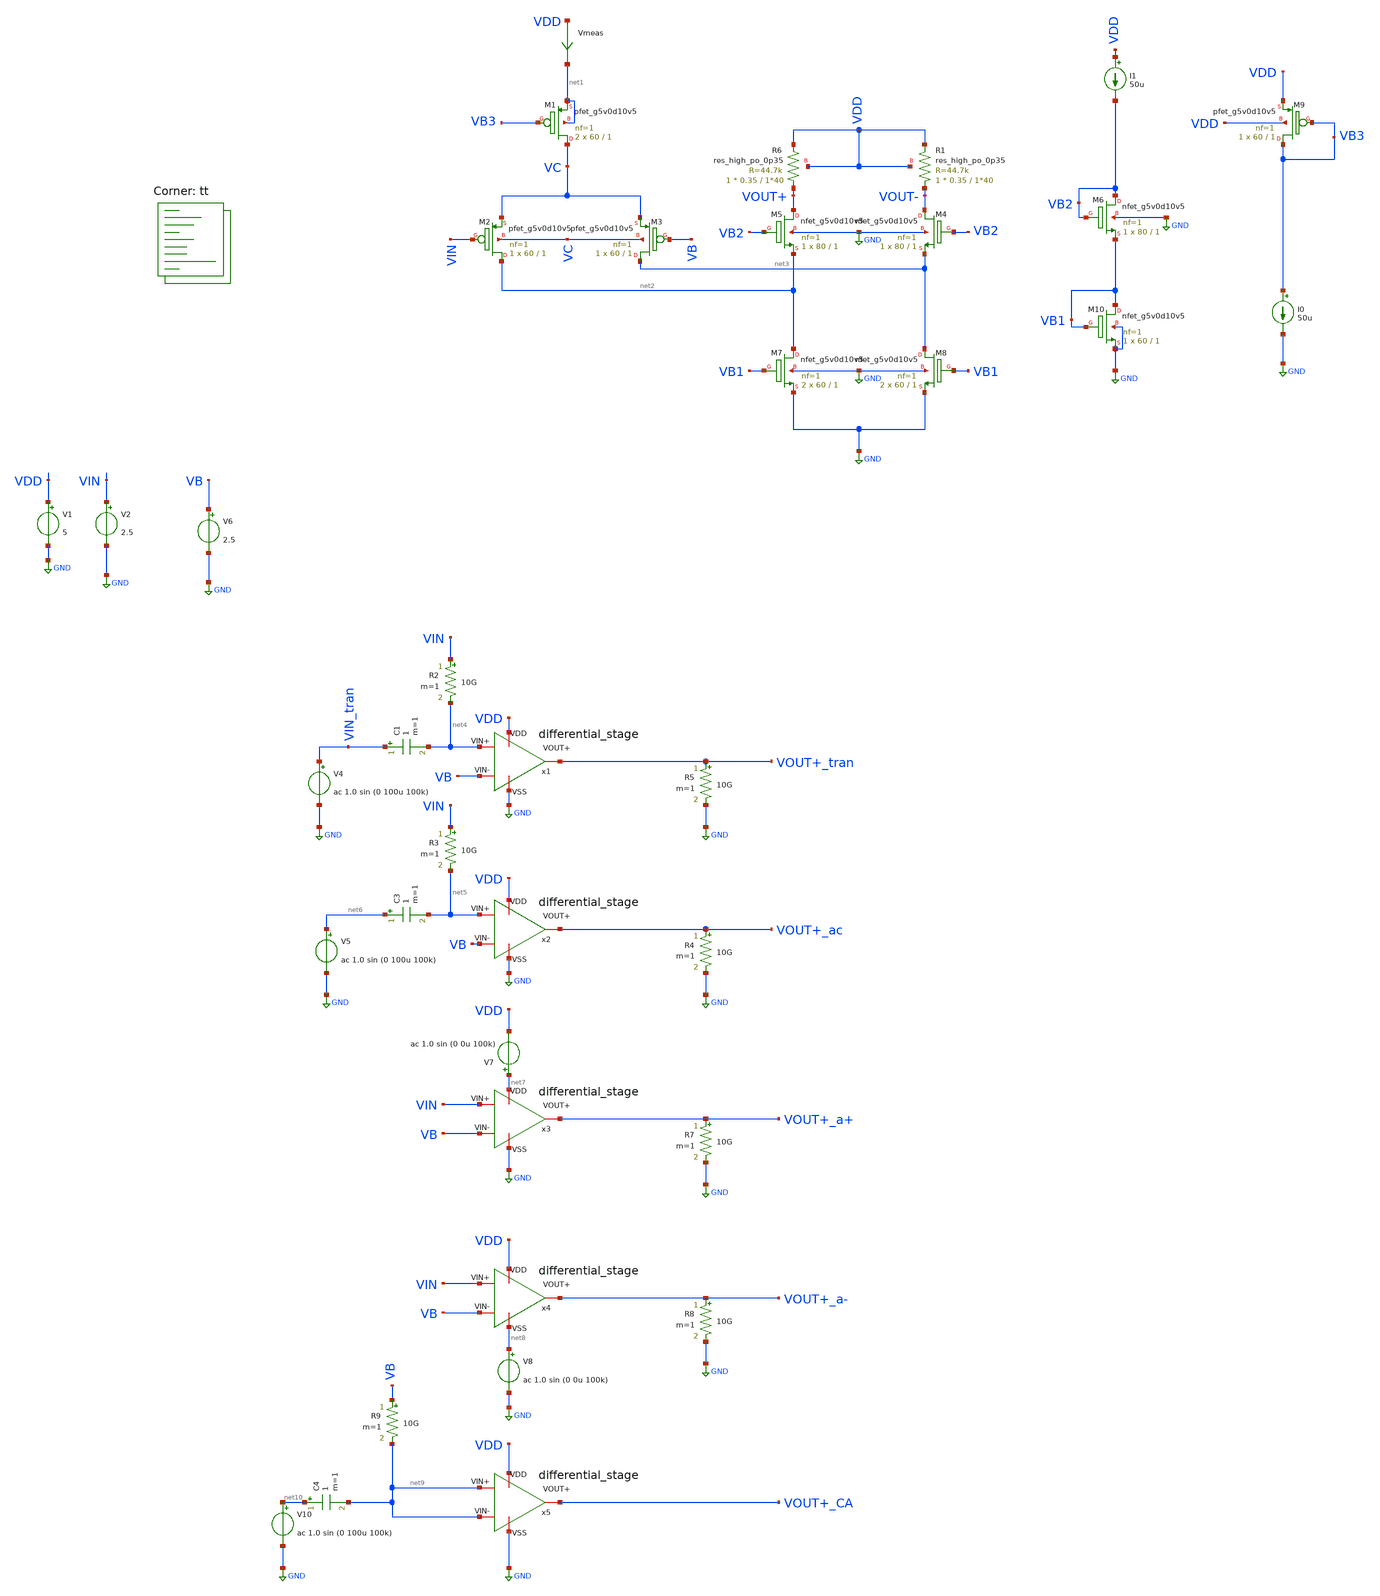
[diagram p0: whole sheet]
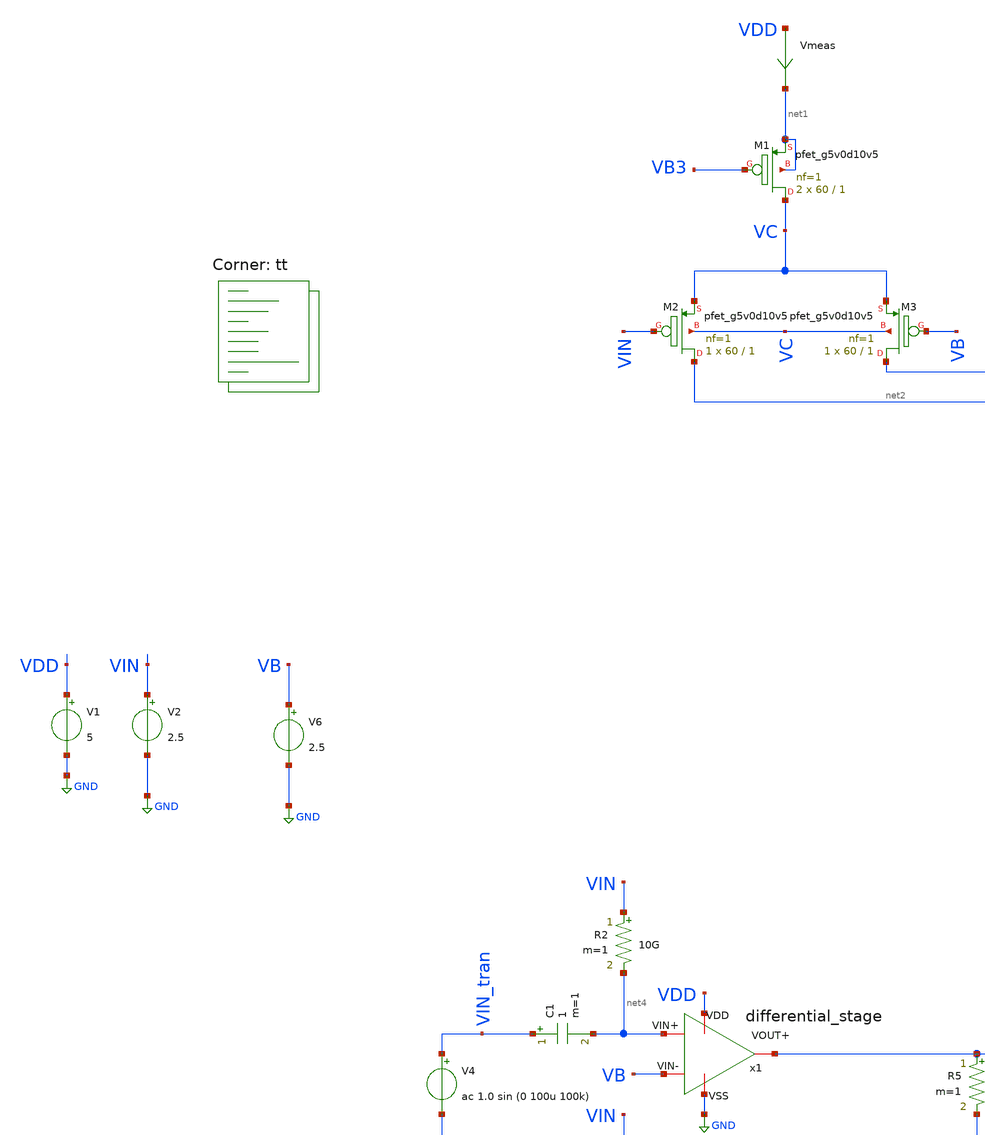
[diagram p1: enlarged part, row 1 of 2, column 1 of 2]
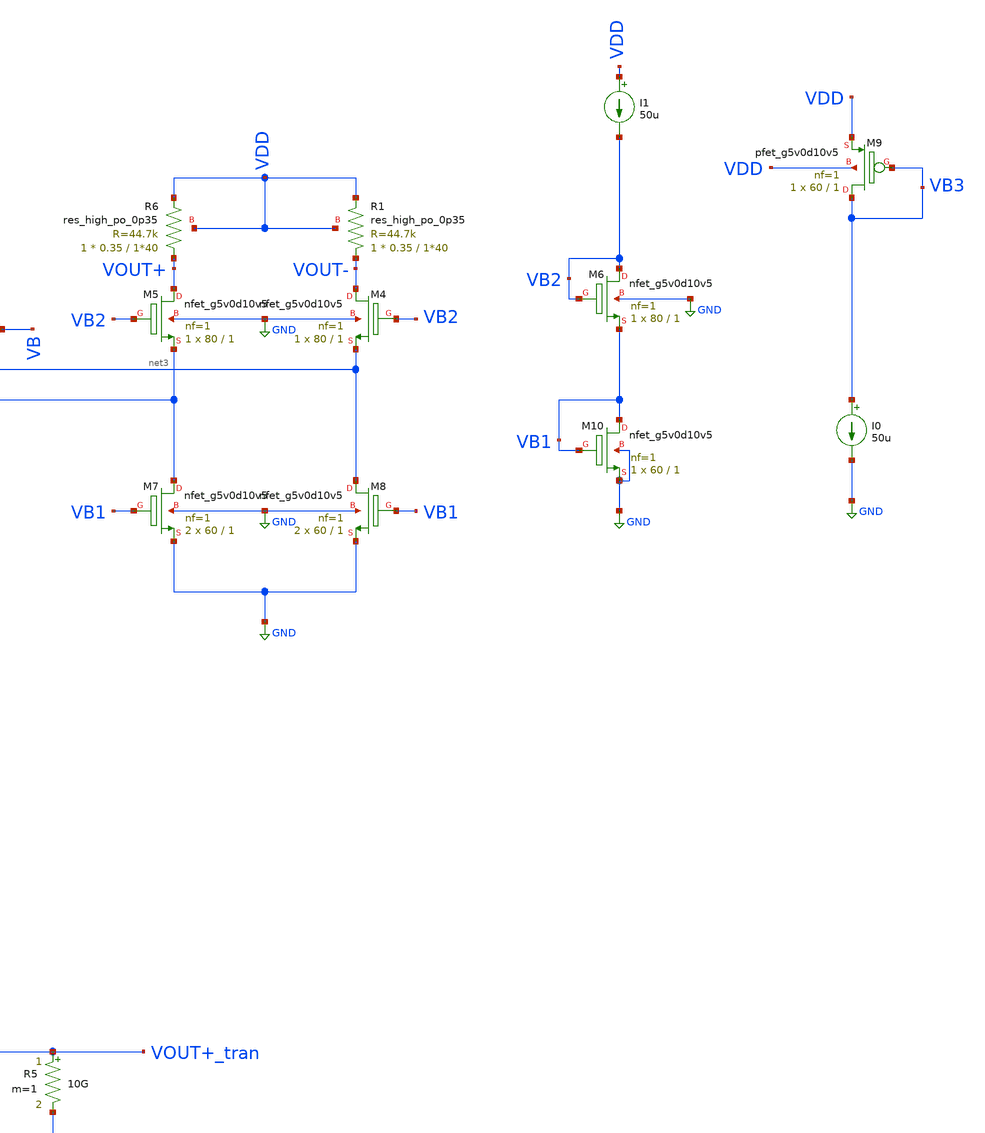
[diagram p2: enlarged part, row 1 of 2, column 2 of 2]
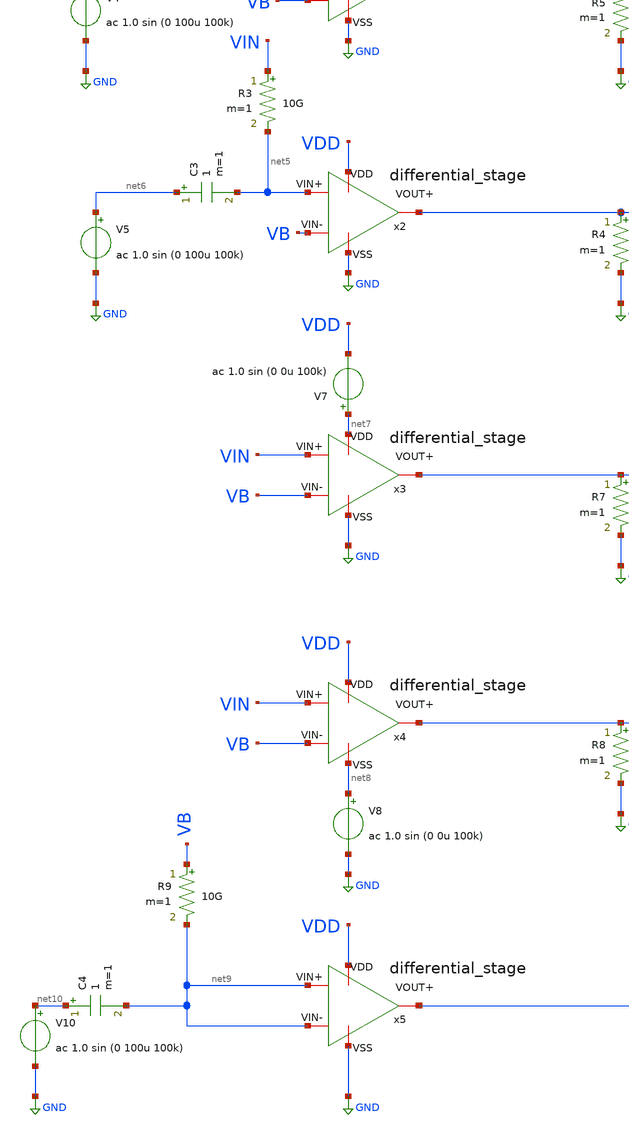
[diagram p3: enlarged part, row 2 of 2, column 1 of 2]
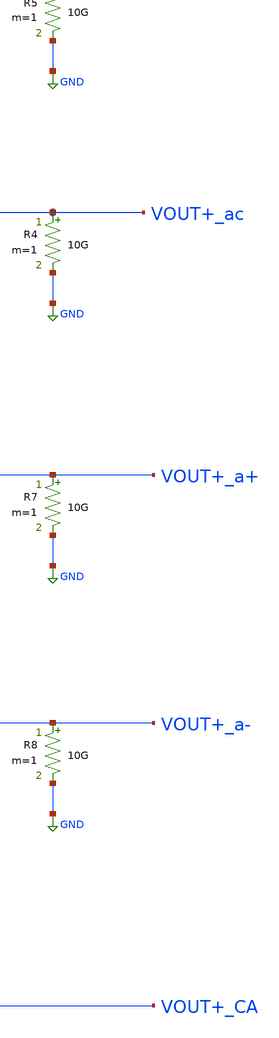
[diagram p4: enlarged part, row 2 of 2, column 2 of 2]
** sch_path: old stuff/amplifiers/differencial_stage_amps/stange stages/folded_cascode/diferential_stage.sch
**.subckt diferential_stage
I0 VB3 GND 50u
Vmeas VDD net1 0
.save i(vmeas)
XM9 VB3 VB3 VDD VDD sky130_fd_pr__pfet_g5v0d10v5 L=1 W=60 nf=1 ad='int((1 + 1)/2) * 60 / 1 * 0.29' as='int((1 + 2)/2) * 60 / 1 * 0.29'
+ pd='2*int((1 + 1)/2) * (60 / 1 + 0.29)' ps='2*int((1 + 2)/2) * (60 / 1 + 0.29)' nrd='0.29 / 60 ' nrs='0.29 / 60 '
+ sa=0 sb=0 sd=0 mult=1 m=1
XM1 VC VB3 net1 net1 sky130_fd_pr__pfet_g5v0d10v5 L=1 W=60 nf=1 ad='int((1 + 1)/2) * 60 / 1 * 0.29' as='int((1 + 2)/2) * 60 / 1 * 0.29'
+ pd='2*int((1 + 1)/2) * (60 / 1 + 0.29)' ps='2*int((1 + 2)/2) * (60 / 1 + 0.29)' nrd='0.29 / 60 ' nrs='0.29 / 60 '
+ sa=0 sb=0 sd=0 mult=2 m=2
XM2 net2 VIN VC VC sky130_fd_pr__pfet_g5v0d10v5 L=1 W=60 nf=1 ad='int((1 + 1)/2) * 60 / 1 * 0.29' as='int((1 + 2)/2) * 60 / 1 * 0.29'
+ pd='2*int((1 + 1)/2) * (60 / 1 + 0.29)' ps='2*int((1 + 2)/2) * (60 / 1 + 0.29)' nrd='0.29 / 60 ' nrs='0.29 / 60 '
+ sa=0 sb=0 sd=0 mult=1 m=1
XM3 net3 VB VC VC sky130_fd_pr__pfet_g5v0d10v5 L=1 W=60 nf=1 ad='int((1 + 1)/2) * 60 / 1 * 0.29' as='int((1 + 2)/2) * 60 / 1 * 0.29'
+ pd='2*int((1 + 1)/2) * (60 / 1 + 0.29)' ps='2*int((1 + 2)/2) * (60 / 1 + 0.29)' nrd='0.29 / 60 ' nrs='0.29 / 60 '
+ sa=0 sb=0 sd=0 mult=1 m=1
XR6 VOUT+ VDD VDD sky130_fd_pr__res_high_po_0p35 L=1*40 mult=1 m=1
XR1 VOUT- VDD VDD sky130_fd_pr__res_high_po_0p35 L=1*40 mult=1 m=1
XM5 VOUT+ VB2 net2 GND sky130_fd_pr__nfet_g5v0d10v5 L=1 W=80 nf=1 ad='int((1 + 1)/2) * 80 / 1 * 0.29'
+ as='int((1 + 2)/2) * 80 / 1 * 0.29' pd='2*int((1 + 1)/2) * (80 / 1 + 0.29)' ps='2*int((1 + 2)/2) * (80 / 1 + 0.29)'
+ nrd='0.29 / 80 ' nrs='0.29 / 80 ' sa=0 sb=0 sd=0 mult=1 m=1
XM4 VOUT- VB2 net3 GND sky130_fd_pr__nfet_g5v0d10v5 L=1 W=80 nf=1 ad='int((1 + 1)/2) * 80 / 1 * 0.29'
+ as='int((1 + 2)/2) * 80 / 1 * 0.29' pd='2*int((1 + 1)/2) * (80 / 1 + 0.29)' ps='2*int((1 + 2)/2) * (80 / 1 + 0.29)'
+ nrd='0.29 / 80 ' nrs='0.29 / 80 ' sa=0 sb=0 sd=0 mult=1 m=1
I1 VDD VB2 50u
XM6 VB2 VB2 VB1 GND sky130_fd_pr__nfet_g5v0d10v5 L=1 W=80 nf=1 ad='int((1 + 1)/2) * 80 / 1 * 0.29' as='int((1 + 2)/2) * 80 / 1 * 0.29'
+ pd='2*int((1 + 1)/2) * (80 / 1 + 0.29)' ps='2*int((1 + 2)/2) * (80 / 1 + 0.29)' nrd='0.29 / 80 ' nrs='0.29 / 80 '
+ sa=0 sb=0 sd=0 mult=1 m=1
XM7 net2 VB1 GND GND sky130_fd_pr__nfet_g5v0d10v5 L=1 W=60 nf=1 ad='int((1 + 1)/2) * 60 / 1 * 0.29' as='int((1 + 2)/2) * 60 / 1 * 0.29'
+ pd='2*int((1 + 1)/2) * (60 / 1 + 0.29)' ps='2*int((1 + 2)/2) * (60 / 1 + 0.29)' nrd='0.29 / 60 ' nrs='0.29 / 60 '
+ sa=0 sb=0 sd=0 mult=2 m=2
XM8 net3 VB1 GND GND sky130_fd_pr__nfet_g5v0d10v5 L=1 W=60 nf=1 ad='int((1 + 1)/2) * 60 / 1 * 0.29' as='int((1 + 2)/2) * 60 / 1 * 0.29'
+ pd='2*int((1 + 1)/2) * (60 / 1 + 0.29)' ps='2*int((1 + 2)/2) * (60 / 1 + 0.29)' nrd='0.29 / 60 ' nrs='0.29 / 60 '
+ sa=0 sb=0 sd=0 mult=2 m=2
XM10 VB1 VB1 GND GND sky130_fd_pr__nfet_g5v0d10v5 L=1 W=60 nf=1 ad='int((1 + 1)/2) * 60 / 1 * 0.29' as='int((1 + 2)/2) * 60 / 1 * 0.29'
+ pd='2*int((1 + 1)/2) * (60 / 1 + 0.29)' ps='2*int((1 + 2)/2) * (60 / 1 + 0.29)' nrd='0.29 / 60 ' nrs='0.29 / 60 '
+ sa=0 sb=0 sd=0 mult=1 m=1
V1 VDD GND 5
V2 VIN GND 2.5
V6 VB GND 2.5
R5 VOUT+_tran GND 10G m=1
R2 VIN net4 10G m=1
V4 VIN_tran GND ac 1.0 sin (0 100u 100k)
C1 VIN_tran net4 1 m=1
R3 VIN net5 10G m=1
C3 net6 net5 1 m=1
V5 net6 GND ac 1.0 sin (0 100u 100k)
R4 VOUT+_ac GND 10G m=1
V7 net7 VDD ac 1.0 sin (0 0u 100k)
R7 VOUT+_a+ GND 10G m=1
V8 net8 GND ac 1.0 sin (0 0u 100k)
R8 VOUT+_a- GND 10G m=1
R9 VB net9 10G m=1
C4 net10 net9 1 m=1
V10 net10 GND ac 1.0 sin (0 100u 100k)
x1 VDD GND net4 VB VOUT+_tran differential_stage
x2 VDD GND net5 VB VOUT+_ac differential_stage
x3 net7 GND VIN VB VOUT+_a+ differential_stage
x4 VDD net8 VIN VB VOUT+_a- differential_stage
x5 VDD GND net9 net9 VOUT+_CA differential_stage
**** begin user architecture code

**************************************************************
**************************************************************
**************************************************************
**************************************************************
**************************************************************
*LIBs*********************************************************
**************************************************************
**************************************************************
**************************************************************
**************************************************************
**************************************************************
*.lib $::SKYWATER_MODELS/sky130.lib.spice tt
* chose the corners in the corner file
* tt_mm for mismatch
* ss ff sf fs standart corners
* ll hh lh hl capacitor and resistors corners
* mc for total process variation including corners
**************************************************************
**************************************************************
**************************************************************
**************************************************************
**************************************************************
*Corners/montecarlo options***********************************
**************************************************************
**************************************************************
**************************************************************
**************************************************************
**************************************************************
.TEMP 27
**************************************************************
**************************************************************
**************************************************************
**************************************************************
*SIMULATION and Plots*****************************************
**************************************************************
**************************************************************
**************************************************************
**************************************************************
.control
save all
dc V2 0 5 0.01
*dc simulation
plot v(VOUT-) v(VIN) deriv(v(VOUT-)) v(VOUT+) deriv(v(VOUT+))
*ploting VIN VOUT and the voltage gain
plot i(Vmeas)
plot -i(v1)
*ploting the current for curiosity
tran 1ns 20u
*transient simulation
plot (v(VOUT+_tran))
*simple plot to exemplify the gain
fft v(VOUT+_tran) v(VIN_tran)
*fast fourier transfor
plot mag(v(VOUT+_tran)) mag(v(VIN_tran))
ac dec 20 1 1000G
*simple ac simulation
plot db(v(VOUT+_ac))
plot db(v(VOUT+_a+))
plot db(v(VOUT+_a-))
plot db(v(VOUT+_CA))
plot db((v(VOUT+_ac))/(v(VOUT+_CA)))
plot db((v(VOUT+_ac))/(v(VOUT+_a+)))
plot db((v(VOUT+_ac))/(v(VOUT+_a-)))
.endc

.lib $::SKYWATER_MODELS/sky130.lib.spice tt
**** end user architecture code
**.ends
.GLOBAL GND
.end
